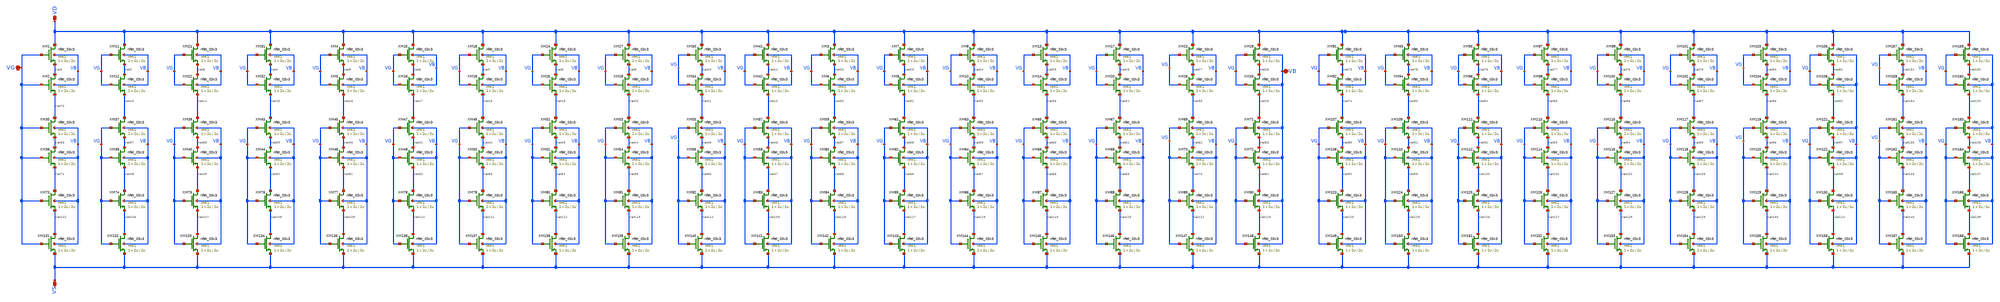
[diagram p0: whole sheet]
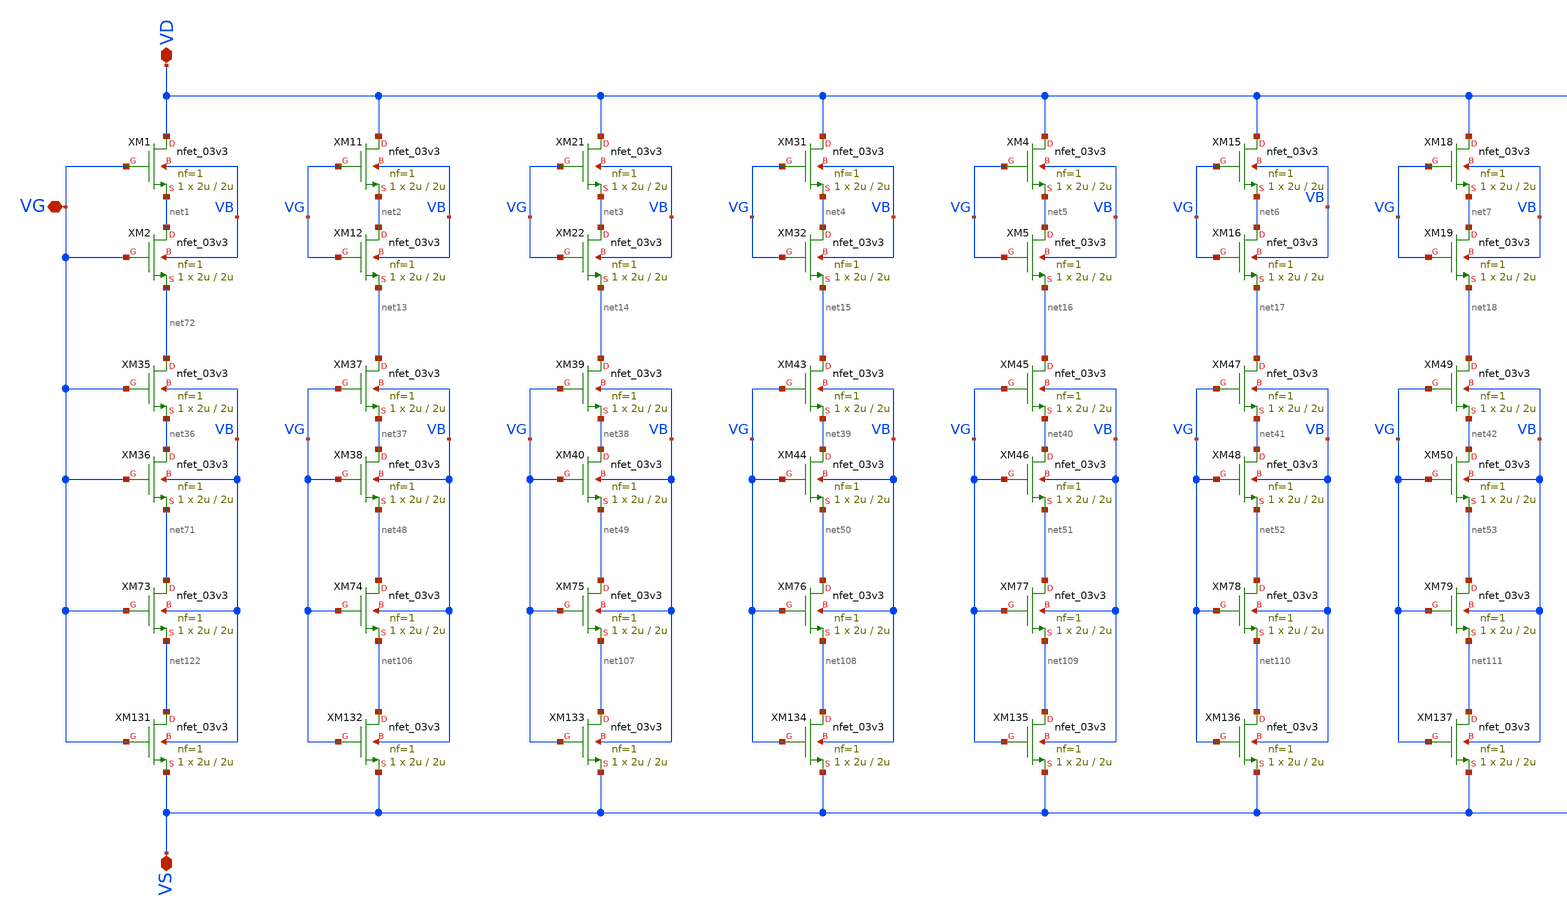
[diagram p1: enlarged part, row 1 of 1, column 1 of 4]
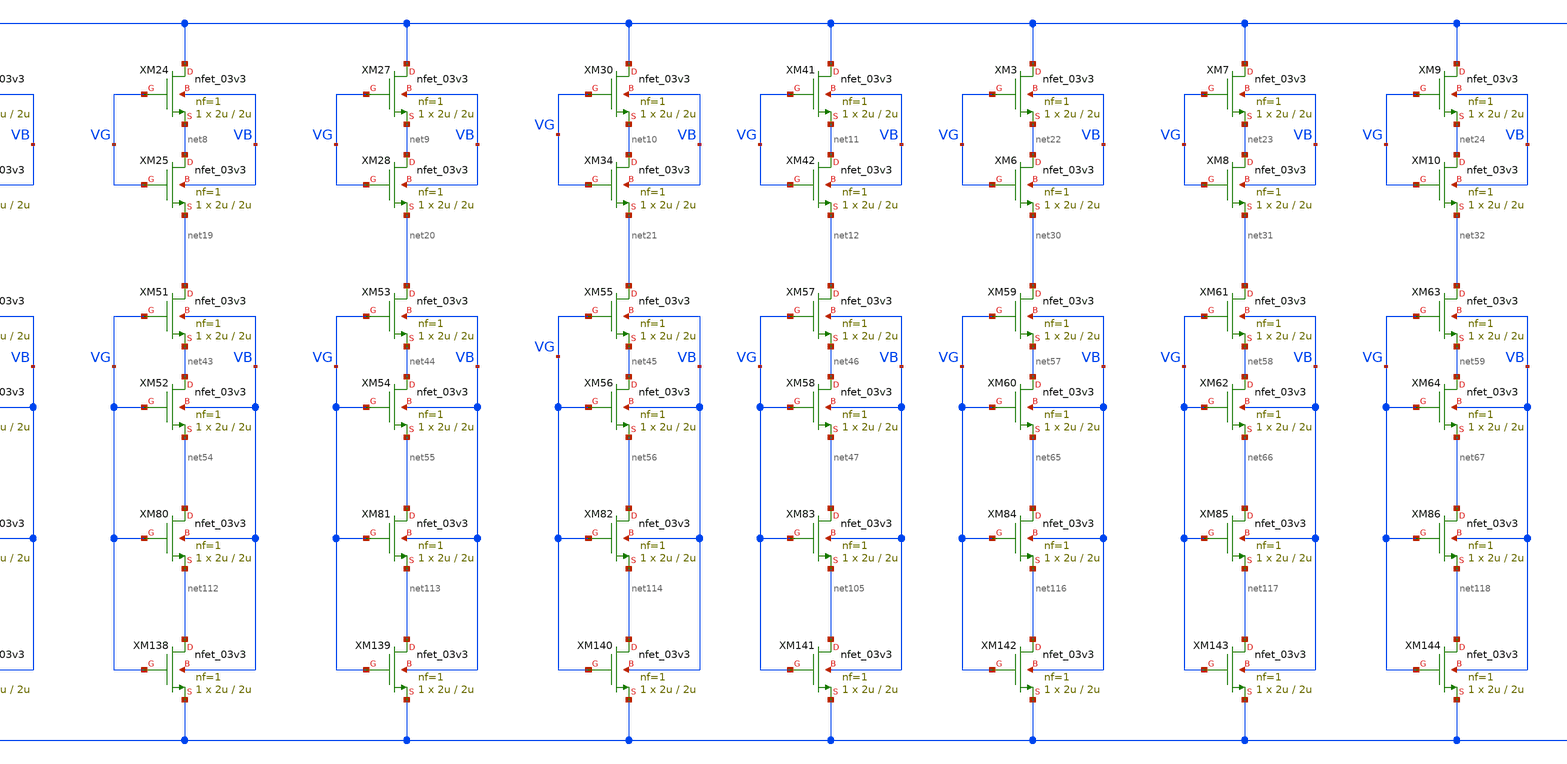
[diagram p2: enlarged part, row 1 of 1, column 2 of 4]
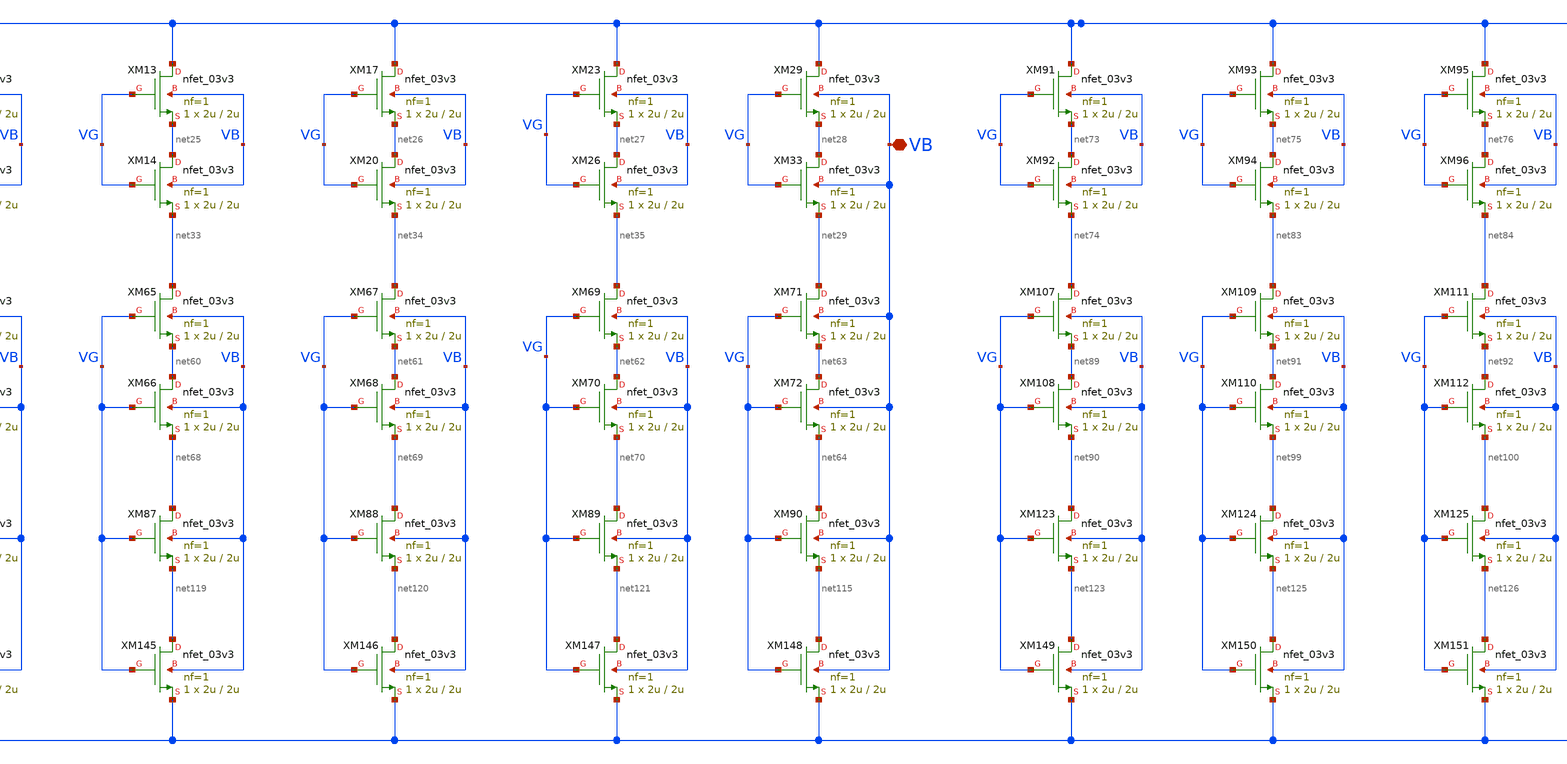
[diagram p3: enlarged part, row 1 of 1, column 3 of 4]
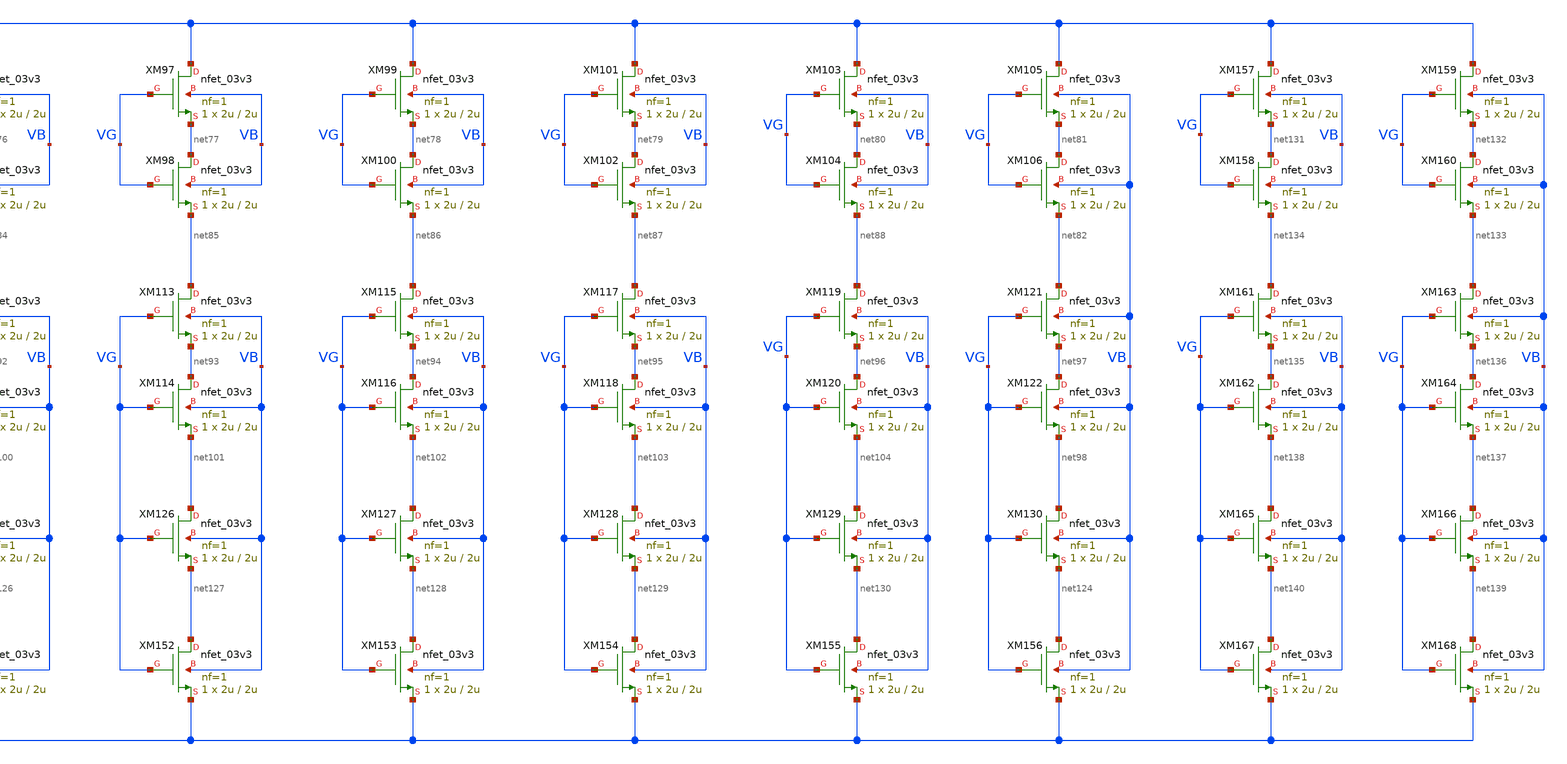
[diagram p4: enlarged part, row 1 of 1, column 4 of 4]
** sch_path: Voltage_Reference/symbols/NMOS_association_18u_5u.sch
**.subckt NMOS_association_18u_5u VD VG VS VB
*.iopin VD
*.iopin VG
*.iopin VS
*.iopin VB
XM1 VD VG net1 VB nfet_03v3 L=2u W=2u nf=1 ad='int((nf+1)/2) * W/nf * 0.18u' as='int((nf+2)/2) * W/nf * 0.18u'
+ pd='2*int((nf+1)/2) * (W/nf + 0.18u)' ps='2*int((nf+2)/2) * (W/nf + 0.18u)' nrd='0.18u / W' nrs='0.18u / W'
+ sa=0 sb=0 sd=0 m=1
XM2 net1 VG net72 VB nfet_03v3 L=2u W=2u nf=1 ad='int((nf+1)/2) * W/nf * 0.18u' as='int((nf+2)/2) * W/nf * 0.18u'
+ pd='2*int((nf+1)/2) * (W/nf + 0.18u)' ps='2*int((nf+2)/2) * (W/nf + 0.18u)' nrd='0.18u / W' nrs='0.18u / W'
+ sa=0 sb=0 sd=0 m=1
XM11 VD VG net2 VB nfet_03v3 L=2u W=2u nf=1 ad='int((nf+1)/2) * W/nf * 0.18u' as='int((nf+2)/2) * W/nf * 0.18u'
+ pd='2*int((nf+1)/2) * (W/nf + 0.18u)' ps='2*int((nf+2)/2) * (W/nf + 0.18u)' nrd='0.18u / W' nrs='0.18u / W'
+ sa=0 sb=0 sd=0 m=1
XM12 net2 VG net13 VB nfet_03v3 L=2u W=2u nf=1 ad='int((nf+1)/2) * W/nf * 0.18u' as='int((nf+2)/2) * W/nf * 0.18u'
+ pd='2*int((nf+1)/2) * (W/nf + 0.18u)' ps='2*int((nf+2)/2) * (W/nf + 0.18u)' nrd='0.18u / W' nrs='0.18u / W'
+ sa=0 sb=0 sd=0 m=1
XM21 VD VG net3 VB nfet_03v3 L=2u W=2u nf=1 ad='int((nf+1)/2) * W/nf * 0.18u' as='int((nf+2)/2) * W/nf * 0.18u'
+ pd='2*int((nf+1)/2) * (W/nf + 0.18u)' ps='2*int((nf+2)/2) * (W/nf + 0.18u)' nrd='0.18u / W' nrs='0.18u / W'
+ sa=0 sb=0 sd=0 m=1
XM22 net3 VG net14 VB nfet_03v3 L=2u W=2u nf=1 ad='int((nf+1)/2) * W/nf * 0.18u' as='int((nf+2)/2) * W/nf * 0.18u'
+ pd='2*int((nf+1)/2) * (W/nf + 0.18u)' ps='2*int((nf+2)/2) * (W/nf + 0.18u)' nrd='0.18u / W' nrs='0.18u / W'
+ sa=0 sb=0 sd=0 m=1
XM31 VD VG net4 VB nfet_03v3 L=2u W=2u nf=1 ad='int((nf+1)/2) * W/nf * 0.18u' as='int((nf+2)/2) * W/nf * 0.18u'
+ pd='2*int((nf+1)/2) * (W/nf + 0.18u)' ps='2*int((nf+2)/2) * (W/nf + 0.18u)' nrd='0.18u / W' nrs='0.18u / W'
+ sa=0 sb=0 sd=0 m=1
XM32 net4 VG net15 VB nfet_03v3 L=2u W=2u nf=1 ad='int((nf+1)/2) * W/nf * 0.18u' as='int((nf+2)/2) * W/nf * 0.18u'
+ pd='2*int((nf+1)/2) * (W/nf + 0.18u)' ps='2*int((nf+2)/2) * (W/nf + 0.18u)' nrd='0.18u / W' nrs='0.18u / W'
+ sa=0 sb=0 sd=0 m=1
XM4 VD VG net5 VB nfet_03v3 L=2u W=2u nf=1 ad='int((nf+1)/2) * W/nf * 0.18u' as='int((nf+2)/2) * W/nf * 0.18u'
+ pd='2*int((nf+1)/2) * (W/nf + 0.18u)' ps='2*int((nf+2)/2) * (W/nf + 0.18u)' nrd='0.18u / W' nrs='0.18u / W'
+ sa=0 sb=0 sd=0 m=1
XM5 net5 VG net16 VB nfet_03v3 L=2u W=2u nf=1 ad='int((nf+1)/2) * W/nf * 0.18u' as='int((nf+2)/2) * W/nf * 0.18u'
+ pd='2*int((nf+1)/2) * (W/nf + 0.18u)' ps='2*int((nf+2)/2) * (W/nf + 0.18u)' nrd='0.18u / W' nrs='0.18u / W'
+ sa=0 sb=0 sd=0 m=1
XM15 VD VG net6 VB nfet_03v3 L=2u W=2u nf=1 ad='int((nf+1)/2) * W/nf * 0.18u' as='int((nf+2)/2) * W/nf * 0.18u'
+ pd='2*int((nf+1)/2) * (W/nf + 0.18u)' ps='2*int((nf+2)/2) * (W/nf + 0.18u)' nrd='0.18u / W' nrs='0.18u / W'
+ sa=0 sb=0 sd=0 m=1
XM16 net6 VG net17 VB nfet_03v3 L=2u W=2u nf=1 ad='int((nf+1)/2) * W/nf * 0.18u' as='int((nf+2)/2) * W/nf * 0.18u'
+ pd='2*int((nf+1)/2) * (W/nf + 0.18u)' ps='2*int((nf+2)/2) * (W/nf + 0.18u)' nrd='0.18u / W' nrs='0.18u / W'
+ sa=0 sb=0 sd=0 m=1
XM18 VD VG net7 VB nfet_03v3 L=2u W=2u nf=1 ad='int((nf+1)/2) * W/nf * 0.18u' as='int((nf+2)/2) * W/nf * 0.18u'
+ pd='2*int((nf+1)/2) * (W/nf + 0.18u)' ps='2*int((nf+2)/2) * (W/nf + 0.18u)' nrd='0.18u / W' nrs='0.18u / W'
+ sa=0 sb=0 sd=0 m=1
XM19 net7 VG net18 VB nfet_03v3 L=2u W=2u nf=1 ad='int((nf+1)/2) * W/nf * 0.18u' as='int((nf+2)/2) * W/nf * 0.18u'
+ pd='2*int((nf+1)/2) * (W/nf + 0.18u)' ps='2*int((nf+2)/2) * (W/nf + 0.18u)' nrd='0.18u / W' nrs='0.18u / W'
+ sa=0 sb=0 sd=0 m=1
XM24 VD VG net8 VB nfet_03v3 L=2u W=2u nf=1 ad='int((nf+1)/2) * W/nf * 0.18u' as='int((nf+2)/2) * W/nf * 0.18u'
+ pd='2*int((nf+1)/2) * (W/nf + 0.18u)' ps='2*int((nf+2)/2) * (W/nf + 0.18u)' nrd='0.18u / W' nrs='0.18u / W'
+ sa=0 sb=0 sd=0 m=1
XM25 net8 VG net19 VB nfet_03v3 L=2u W=2u nf=1 ad='int((nf+1)/2) * W/nf * 0.18u' as='int((nf+2)/2) * W/nf * 0.18u'
+ pd='2*int((nf+1)/2) * (W/nf + 0.18u)' ps='2*int((nf+2)/2) * (W/nf + 0.18u)' nrd='0.18u / W' nrs='0.18u / W'
+ sa=0 sb=0 sd=0 m=1
XM27 VD VG net9 VB nfet_03v3 L=2u W=2u nf=1 ad='int((nf+1)/2) * W/nf * 0.18u' as='int((nf+2)/2) * W/nf * 0.18u'
+ pd='2*int((nf+1)/2) * (W/nf + 0.18u)' ps='2*int((nf+2)/2) * (W/nf + 0.18u)' nrd='0.18u / W' nrs='0.18u / W'
+ sa=0 sb=0 sd=0 m=1
XM28 net9 VG net20 VB nfet_03v3 L=2u W=2u nf=1 ad='int((nf+1)/2) * W/nf * 0.18u' as='int((nf+2)/2) * W/nf * 0.18u'
+ pd='2*int((nf+1)/2) * (W/nf + 0.18u)' ps='2*int((nf+2)/2) * (W/nf + 0.18u)' nrd='0.18u / W' nrs='0.18u / W'
+ sa=0 sb=0 sd=0 m=1
XM30 VD VG net10 VB nfet_03v3 L=2u W=2u nf=1 ad='int((nf+1)/2) * W/nf * 0.18u' as='int((nf+2)/2) * W/nf * 0.18u'
+ pd='2*int((nf+1)/2) * (W/nf + 0.18u)' ps='2*int((nf+2)/2) * (W/nf + 0.18u)' nrd='0.18u / W' nrs='0.18u / W'
+ sa=0 sb=0 sd=0 m=1
XM34 net10 VG net21 VB nfet_03v3 L=2u W=2u nf=1 ad='int((nf+1)/2) * W/nf * 0.18u' as='int((nf+2)/2) * W/nf * 0.18u'
+ pd='2*int((nf+1)/2) * (W/nf + 0.18u)' ps='2*int((nf+2)/2) * (W/nf + 0.18u)' nrd='0.18u / W' nrs='0.18u / W'
+ sa=0 sb=0 sd=0 m=1
XM41 VD VG net11 VB nfet_03v3 L=2u W=2u nf=1 ad='int((nf+1)/2) * W/nf * 0.18u' as='int((nf+2)/2) * W/nf * 0.18u'
+ pd='2*int((nf+1)/2) * (W/nf + 0.18u)' ps='2*int((nf+2)/2) * (W/nf + 0.18u)' nrd='0.18u / W' nrs='0.18u / W'
+ sa=0 sb=0 sd=0 m=1
XM42 net11 VG net12 VB nfet_03v3 L=2u W=2u nf=1 ad='int((nf+1)/2) * W/nf * 0.18u' as='int((nf+2)/2) * W/nf * 0.18u'
+ pd='2*int((nf+1)/2) * (W/nf + 0.18u)' ps='2*int((nf+2)/2) * (W/nf + 0.18u)' nrd='0.18u / W' nrs='0.18u / W'
+ sa=0 sb=0 sd=0 m=1
XM3 VD VG net22 VB nfet_03v3 L=2u W=2u nf=1 ad='int((nf+1)/2) * W/nf * 0.18u' as='int((nf+2)/2) * W/nf * 0.18u'
+ pd='2*int((nf+1)/2) * (W/nf + 0.18u)' ps='2*int((nf+2)/2) * (W/nf + 0.18u)' nrd='0.18u / W' nrs='0.18u / W'
+ sa=0 sb=0 sd=0 m=1
XM6 net22 VG net30 VB nfet_03v3 L=2u W=2u nf=1 ad='int((nf+1)/2) * W/nf * 0.18u' as='int((nf+2)/2) * W/nf * 0.18u'
+ pd='2*int((nf+1)/2) * (W/nf + 0.18u)' ps='2*int((nf+2)/2) * (W/nf + 0.18u)' nrd='0.18u / W' nrs='0.18u / W'
+ sa=0 sb=0 sd=0 m=1
XM7 VD VG net23 VB nfet_03v3 L=2u W=2u nf=1 ad='int((nf+1)/2) * W/nf * 0.18u' as='int((nf+2)/2) * W/nf * 0.18u'
+ pd='2*int((nf+1)/2) * (W/nf + 0.18u)' ps='2*int((nf+2)/2) * (W/nf + 0.18u)' nrd='0.18u / W' nrs='0.18u / W'
+ sa=0 sb=0 sd=0 m=1
XM8 net23 VG net31 VB nfet_03v3 L=2u W=2u nf=1 ad='int((nf+1)/2) * W/nf * 0.18u' as='int((nf+2)/2) * W/nf * 0.18u'
+ pd='2*int((nf+1)/2) * (W/nf + 0.18u)' ps='2*int((nf+2)/2) * (W/nf + 0.18u)' nrd='0.18u / W' nrs='0.18u / W'
+ sa=0 sb=0 sd=0 m=1
XM9 VD VG net24 VB nfet_03v3 L=2u W=2u nf=1 ad='int((nf+1)/2) * W/nf * 0.18u' as='int((nf+2)/2) * W/nf * 0.18u'
+ pd='2*int((nf+1)/2) * (W/nf + 0.18u)' ps='2*int((nf+2)/2) * (W/nf + 0.18u)' nrd='0.18u / W' nrs='0.18u / W'
+ sa=0 sb=0 sd=0 m=1
XM10 net24 VG net32 VB nfet_03v3 L=2u W=2u nf=1 ad='int((nf+1)/2) * W/nf * 0.18u' as='int((nf+2)/2) * W/nf * 0.18u'
+ pd='2*int((nf+1)/2) * (W/nf + 0.18u)' ps='2*int((nf+2)/2) * (W/nf + 0.18u)' nrd='0.18u / W' nrs='0.18u / W'
+ sa=0 sb=0 sd=0 m=1
XM13 VD VG net25 VB nfet_03v3 L=2u W=2u nf=1 ad='int((nf+1)/2) * W/nf * 0.18u' as='int((nf+2)/2) * W/nf * 0.18u'
+ pd='2*int((nf+1)/2) * (W/nf + 0.18u)' ps='2*int((nf+2)/2) * (W/nf + 0.18u)' nrd='0.18u / W' nrs='0.18u / W'
+ sa=0 sb=0 sd=0 m=1
XM14 net25 VG net33 VB nfet_03v3 L=2u W=2u nf=1 ad='int((nf+1)/2) * W/nf * 0.18u' as='int((nf+2)/2) * W/nf * 0.18u'
+ pd='2*int((nf+1)/2) * (W/nf + 0.18u)' ps='2*int((nf+2)/2) * (W/nf + 0.18u)' nrd='0.18u / W' nrs='0.18u / W'
+ sa=0 sb=0 sd=0 m=1
XM17 VD VG net26 VB nfet_03v3 L=2u W=2u nf=1 ad='int((nf+1)/2) * W/nf * 0.18u' as='int((nf+2)/2) * W/nf * 0.18u'
+ pd='2*int((nf+1)/2) * (W/nf + 0.18u)' ps='2*int((nf+2)/2) * (W/nf + 0.18u)' nrd='0.18u / W' nrs='0.18u / W'
+ sa=0 sb=0 sd=0 m=1
XM20 net26 VG net34 VB nfet_03v3 L=2u W=2u nf=1 ad='int((nf+1)/2) * W/nf * 0.18u' as='int((nf+2)/2) * W/nf * 0.18u'
+ pd='2*int((nf+1)/2) * (W/nf + 0.18u)' ps='2*int((nf+2)/2) * (W/nf + 0.18u)' nrd='0.18u / W' nrs='0.18u / W'
+ sa=0 sb=0 sd=0 m=1
XM23 VD VG net27 VB nfet_03v3 L=2u W=2u nf=1 ad='int((nf+1)/2) * W/nf * 0.18u' as='int((nf+2)/2) * W/nf * 0.18u'
+ pd='2*int((nf+1)/2) * (W/nf + 0.18u)' ps='2*int((nf+2)/2) * (W/nf + 0.18u)' nrd='0.18u / W' nrs='0.18u / W'
+ sa=0 sb=0 sd=0 m=1
XM26 net27 VG net35 VB nfet_03v3 L=2u W=2u nf=1 ad='int((nf+1)/2) * W/nf * 0.18u' as='int((nf+2)/2) * W/nf * 0.18u'
+ pd='2*int((nf+1)/2) * (W/nf + 0.18u)' ps='2*int((nf+2)/2) * (W/nf + 0.18u)' nrd='0.18u / W' nrs='0.18u / W'
+ sa=0 sb=0 sd=0 m=1
XM29 VD VG net28 VB nfet_03v3 L=2u W=2u nf=1 ad='int((nf+1)/2) * W/nf * 0.18u' as='int((nf+2)/2) * W/nf * 0.18u'
+ pd='2*int((nf+1)/2) * (W/nf + 0.18u)' ps='2*int((nf+2)/2) * (W/nf + 0.18u)' nrd='0.18u / W' nrs='0.18u / W'
+ sa=0 sb=0 sd=0 m=1
XM33 net28 VG net29 VB nfet_03v3 L=2u W=2u nf=1 ad='int((nf+1)/2) * W/nf * 0.18u' as='int((nf+2)/2) * W/nf * 0.18u'
+ pd='2*int((nf+1)/2) * (W/nf + 0.18u)' ps='2*int((nf+2)/2) * (W/nf + 0.18u)' nrd='0.18u / W' nrs='0.18u / W'
+ sa=0 sb=0 sd=0 m=1
XM35 net72 VG net36 VB nfet_03v3 L=2u W=2u nf=1 ad='int((nf+1)/2) * W/nf * 0.18u' as='int((nf+2)/2) * W/nf * 0.18u'
+ pd='2*int((nf+1)/2) * (W/nf + 0.18u)' ps='2*int((nf+2)/2) * (W/nf + 0.18u)' nrd='0.18u / W' nrs='0.18u / W'
+ sa=0 sb=0 sd=0 m=1
XM36 net36 VG net71 VB nfet_03v3 L=2u W=2u nf=1 ad='int((nf+1)/2) * W/nf * 0.18u' as='int((nf+2)/2) * W/nf * 0.18u'
+ pd='2*int((nf+1)/2) * (W/nf + 0.18u)' ps='2*int((nf+2)/2) * (W/nf + 0.18u)' nrd='0.18u / W' nrs='0.18u / W'
+ sa=0 sb=0 sd=0 m=1
XM37 net13 VG net37 VB nfet_03v3 L=2u W=2u nf=1 ad='int((nf+1)/2) * W/nf * 0.18u' as='int((nf+2)/2) * W/nf * 0.18u'
+ pd='2*int((nf+1)/2) * (W/nf + 0.18u)' ps='2*int((nf+2)/2) * (W/nf + 0.18u)' nrd='0.18u / W' nrs='0.18u / W'
+ sa=0 sb=0 sd=0 m=1
XM38 net37 VG net48 VB nfet_03v3 L=2u W=2u nf=1 ad='int((nf+1)/2) * W/nf * 0.18u' as='int((nf+2)/2) * W/nf * 0.18u'
+ pd='2*int((nf+1)/2) * (W/nf + 0.18u)' ps='2*int((nf+2)/2) * (W/nf + 0.18u)' nrd='0.18u / W' nrs='0.18u / W'
+ sa=0 sb=0 sd=0 m=1
XM39 net14 VG net38 VB nfet_03v3 L=2u W=2u nf=1 ad='int((nf+1)/2) * W/nf * 0.18u' as='int((nf+2)/2) * W/nf * 0.18u'
+ pd='2*int((nf+1)/2) * (W/nf + 0.18u)' ps='2*int((nf+2)/2) * (W/nf + 0.18u)' nrd='0.18u / W' nrs='0.18u / W'
+ sa=0 sb=0 sd=0 m=1
XM40 net38 VG net49 VB nfet_03v3 L=2u W=2u nf=1 ad='int((nf+1)/2) * W/nf * 0.18u' as='int((nf+2)/2) * W/nf * 0.18u'
+ pd='2*int((nf+1)/2) * (W/nf + 0.18u)' ps='2*int((nf+2)/2) * (W/nf + 0.18u)' nrd='0.18u / W' nrs='0.18u / W'
+ sa=0 sb=0 sd=0 m=1
XM43 net15 VG net39 VB nfet_03v3 L=2u W=2u nf=1 ad='int((nf+1)/2) * W/nf * 0.18u' as='int((nf+2)/2) * W/nf * 0.18u'
+ pd='2*int((nf+1)/2) * (W/nf + 0.18u)' ps='2*int((nf+2)/2) * (W/nf + 0.18u)' nrd='0.18u / W' nrs='0.18u / W'
+ sa=0 sb=0 sd=0 m=1
XM44 net39 VG net50 VB nfet_03v3 L=2u W=2u nf=1 ad='int((nf+1)/2) * W/nf * 0.18u' as='int((nf+2)/2) * W/nf * 0.18u'
+ pd='2*int((nf+1)/2) * (W/nf + 0.18u)' ps='2*int((nf+2)/2) * (W/nf + 0.18u)' nrd='0.18u / W' nrs='0.18u / W'
+ sa=0 sb=0 sd=0 m=1
XM45 net16 VG net40 VB nfet_03v3 L=2u W=2u nf=1 ad='int((nf+1)/2) * W/nf * 0.18u' as='int((nf+2)/2) * W/nf * 0.18u'
+ pd='2*int((nf+1)/2) * (W/nf + 0.18u)' ps='2*int((nf+2)/2) * (W/nf + 0.18u)' nrd='0.18u / W' nrs='0.18u / W'
+ sa=0 sb=0 sd=0 m=1
XM46 net40 VG net51 VB nfet_03v3 L=2u W=2u nf=1 ad='int((nf+1)/2) * W/nf * 0.18u' as='int((nf+2)/2) * W/nf * 0.18u'
+ pd='2*int((nf+1)/2) * (W/nf + 0.18u)' ps='2*int((nf+2)/2) * (W/nf + 0.18u)' nrd='0.18u / W' nrs='0.18u / W'
+ sa=0 sb=0 sd=0 m=1
XM47 net17 VG net41 VB nfet_03v3 L=2u W=2u nf=1 ad='int((nf+1)/2) * W/nf * 0.18u' as='int((nf+2)/2) * W/nf * 0.18u'
+ pd='2*int((nf+1)/2) * (W/nf + 0.18u)' ps='2*int((nf+2)/2) * (W/nf + 0.18u)' nrd='0.18u / W' nrs='0.18u / W'
+ sa=0 sb=0 sd=0 m=1
XM48 net41 VG net52 VB nfet_03v3 L=2u W=2u nf=1 ad='int((nf+1)/2) * W/nf * 0.18u' as='int((nf+2)/2) * W/nf * 0.18u'
+ pd='2*int((nf+1)/2) * (W/nf + 0.18u)' ps='2*int((nf+2)/2) * (W/nf + 0.18u)' nrd='0.18u / W' nrs='0.18u / W'
+ sa=0 sb=0 sd=0 m=1
XM49 net18 VG net42 VB nfet_03v3 L=2u W=2u nf=1 ad='int((nf+1)/2) * W/nf * 0.18u' as='int((nf+2)/2) * W/nf * 0.18u'
+ pd='2*int((nf+1)/2) * (W/nf + 0.18u)' ps='2*int((nf+2)/2) * (W/nf + 0.18u)' nrd='0.18u / W' nrs='0.18u / W'
+ sa=0 sb=0 sd=0 m=1
XM50 net42 VG net53 VB nfet_03v3 L=2u W=2u nf=1 ad='int((nf+1)/2) * W/nf * 0.18u' as='int((nf+2)/2) * W/nf * 0.18u'
+ pd='2*int((nf+1)/2) * (W/nf + 0.18u)' ps='2*int((nf+2)/2) * (W/nf + 0.18u)' nrd='0.18u / W' nrs='0.18u / W'
+ sa=0 sb=0 sd=0 m=1
XM51 net19 VG net43 VB nfet_03v3 L=2u W=2u nf=1 ad='int((nf+1)/2) * W/nf * 0.18u' as='int((nf+2)/2) * W/nf * 0.18u'
+ pd='2*int((nf+1)/2) * (W/nf + 0.18u)' ps='2*int((nf+2)/2) * (W/nf + 0.18u)' nrd='0.18u / W' nrs='0.18u / W'
+ sa=0 sb=0 sd=0 m=1
XM52 net43 VG net54 VB nfet_03v3 L=2u W=2u nf=1 ad='int((nf+1)/2) * W/nf * 0.18u' as='int((nf+2)/2) * W/nf * 0.18u'
+ pd='2*int((nf+1)/2) * (W/nf + 0.18u)' ps='2*int((nf+2)/2) * (W/nf + 0.18u)' nrd='0.18u / W' nrs='0.18u / W'
+ sa=0 sb=0 sd=0 m=1
XM53 net20 VG net44 VB nfet_03v3 L=2u W=2u nf=1 ad='int((nf+1)/2) * W/nf * 0.18u' as='int((nf+2)/2) * W/nf * 0.18u'
+ pd='2*int((nf+1)/2) * (W/nf + 0.18u)' ps='2*int((nf+2)/2) * (W/nf + 0.18u)' nrd='0.18u / W' nrs='0.18u / W'
+ sa=0 sb=0 sd=0 m=1
XM54 net44 VG net55 VB nfet_03v3 L=2u W=2u nf=1 ad='int((nf+1)/2) * W/nf * 0.18u' as='int((nf+2)/2) * W/nf * 0.18u'
+ pd='2*int((nf+1)/2) * (W/nf + 0.18u)' ps='2*int((nf+2)/2) * (W/nf + 0.18u)' nrd='0.18u / W' nrs='0.18u / W'
+ sa=0 sb=0 sd=0 m=1
XM55 net21 VG net45 VB nfet_03v3 L=2u W=2u nf=1 ad='int((nf+1)/2) * W/nf * 0.18u' as='int((nf+2)/2) * W/nf * 0.18u'
+ pd='2*int((nf+1)/2) * (W/nf + 0.18u)' ps='2*int((nf+2)/2) * (W/nf + 0.18u)' nrd='0.18u / W' nrs='0.18u / W'
+ sa=0 sb=0 sd=0 m=1
XM56 net45 VG net56 VB nfet_03v3 L=2u W=2u nf=1 ad='int((nf+1)/2) * W/nf * 0.18u' as='int((nf+2)/2) * W/nf * 0.18u'
+ pd='2*int((nf+1)/2) * (W/nf + 0.18u)' ps='2*int((nf+2)/2) * (W/nf + 0.18u)' nrd='0.18u / W' nrs='0.18u / W'
+ sa=0 sb=0 sd=0 m=1
XM57 net12 VG net46 VB nfet_03v3 L=2u W=2u nf=1 ad='int((nf+1)/2) * W/nf * 0.18u' as='int((nf+2)/2) * W/nf * 0.18u'
+ pd='2*int((nf+1)/2) * (W/nf + 0.18u)' ps='2*int((nf+2)/2) * (W/nf + 0.18u)' nrd='0.18u / W' nrs='0.18u / W'
+ sa=0 sb=0 sd=0 m=1
XM58 net46 VG net47 VB nfet_03v3 L=2u W=2u nf=1 ad='int((nf+1)/2) * W/nf * 0.18u' as='int((nf+2)/2) * W/nf * 0.18u'
+ pd='2*int((nf+1)/2) * (W/nf + 0.18u)' ps='2*int((nf+2)/2) * (W/nf + 0.18u)' nrd='0.18u / W' nrs='0.18u / W'
+ sa=0 sb=0 sd=0 m=1
XM59 net30 VG net57 VB nfet_03v3 L=2u W=2u nf=1 ad='int((nf+1)/2) * W/nf * 0.18u' as='int((nf+2)/2) * W/nf * 0.18u'
+ pd='2*int((nf+1)/2) * (W/nf + 0.18u)' ps='2*int((nf+2)/2) * (W/nf + 0.18u)' nrd='0.18u / W' nrs='0.18u / W'
+ sa=0 sb=0 sd=0 m=1
XM60 net57 VG net65 VB nfet_03v3 L=2u W=2u nf=1 ad='int((nf+1)/2) * W/nf * 0.18u' as='int((nf+2)/2) * W/nf * 0.18u'
+ pd='2*int((nf+1)/2) * (W/nf + 0.18u)' ps='2*int((nf+2)/2) * (W/nf + 0.18u)' nrd='0.18u / W' nrs='0.18u / W'
+ sa=0 sb=0 sd=0 m=1
XM61 net31 VG net58 VB nfet_03v3 L=2u W=2u nf=1 ad='int((nf+1)/2) * W/nf * 0.18u' as='int((nf+2)/2) * W/nf * 0.18u'
+ pd='2*int((nf+1)/2) * (W/nf + 0.18u)' ps='2*int((nf+2)/2) * (W/nf + 0.18u)' nrd='0.18u / W' nrs='0.18u / W'
+ sa=0 sb=0 sd=0 m=1
XM62 net58 VG net66 VB nfet_03v3 L=2u W=2u nf=1 ad='int((nf+1)/2) * W/nf * 0.18u' as='int((nf+2)/2) * W/nf * 0.18u'
+ pd='2*int((nf+1)/2) * (W/nf + 0.18u)' ps='2*int((nf+2)/2) * (W/nf + 0.18u)' nrd='0.18u / W' nrs='0.18u / W'
+ sa=0 sb=0 sd=0 m=1
XM63 net32 VG net59 VB nfet_03v3 L=2u W=2u nf=1 ad='int((nf+1)/2) * W/nf * 0.18u' as='int((nf+2)/2) * W/nf * 0.18u'
+ pd='2*int((nf+1)/2) * (W/nf + 0.18u)' ps='2*int((nf+2)/2) * (W/nf + 0.18u)' nrd='0.18u / W' nrs='0.18u / W'
+ sa=0 sb=0 sd=0 m=1
XM64 net59 VG net67 VB nfet_03v3 L=2u W=2u nf=1 ad='int((nf+1)/2) * W/nf * 0.18u' as='int((nf+2)/2) * W/nf * 0.18u'
+ pd='2*int((nf+1)/2) * (W/nf + 0.18u)' ps='2*int((nf+2)/2) * (W/nf + 0.18u)' nrd='0.18u / W' nrs='0.18u / W'
+ sa=0 sb=0 sd=0 m=1
XM65 net33 VG net60 VB nfet_03v3 L=2u W=2u nf=1 ad='int((nf+1)/2) * W/nf * 0.18u' as='int((nf+2)/2) * W/nf * 0.18u'
+ pd='2*int((nf+1)/2) * (W/nf + 0.18u)' ps='2*int((nf+2)/2) * (W/nf + 0.18u)' nrd='0.18u / W' nrs='0.18u / W'
+ sa=0 sb=0 sd=0 m=1
XM66 net60 VG net68 VB nfet_03v3 L=2u W=2u nf=1 ad='int((nf+1)/2) * W/nf * 0.18u' as='int((nf+2)/2) * W/nf * 0.18u'
+ pd='2*int((nf+1)/2) * (W/nf + 0.18u)' ps='2*int((nf+2)/2) * (W/nf + 0.18u)' nrd='0.18u / W' nrs='0.18u / W'
+ sa=0 sb=0 sd=0 m=1
XM67 net34 VG net61 VB nfet_03v3 L=2u W=2u nf=1 ad='int((nf+1)/2) * W/nf * 0.18u' as='int((nf+2)/2) * W/nf * 0.18u'
+ pd='2*int((nf+1)/2) * (W/nf + 0.18u)' ps='2*int((nf+2)/2) * (W/nf + 0.18u)' nrd='0.18u / W' nrs='0.18u / W'
+ sa=0 sb=0 sd=0 m=1
XM68 net61 VG net69 VB nfet_03v3 L=2u W=2u nf=1 ad='int((nf+1)/2) * W/nf * 0.18u' as='int((nf+2)/2) * W/nf * 0.18u'
+ pd='2*int((nf+1)/2) * (W/nf + 0.18u)' ps='2*int((nf+2)/2) * (W/nf + 0.18u)' nrd='0.18u / W' nrs='0.18u / W'
+ sa=0 sb=0 sd=0 m=1
XM69 net35 VG net62 VB nfet_03v3 L=2u W=2u nf=1 ad='int((nf+1)/2) * W/nf * 0.18u' as='int((nf+2)/2) * W/nf * 0.18u'
+ pd='2*int((nf+1)/2) * (W/nf + 0.18u)' ps='2*int((nf+2)/2) * (W/nf + 0.18u)' nrd='0.18u / W' nrs='0.18u / W'
+ sa=0 sb=0 sd=0 m=1
XM70 net62 VG net70 VB nfet_03v3 L=2u W=2u nf=1 ad='int((nf+1)/2) * W/nf * 0.18u' as='int((nf+2)/2) * W/nf * 0.18u'
+ pd='2*int((nf+1)/2) * (W/nf + 0.18u)' ps='2*int((nf+2)/2) * (W/nf + 0.18u)' nrd='0.18u / W' nrs='0.18u / W'
+ sa=0 sb=0 sd=0 m=1
XM71 net29 VG net63 VB nfet_03v3 L=2u W=2u nf=1 ad='int((nf+1)/2) * W/nf * 0.18u' as='int((nf+2)/2) * W/nf * 0.18u'
+ pd='2*int((nf+1)/2) * (W/nf + 0.18u)' ps='2*int((nf+2)/2) * (W/nf + 0.18u)' nrd='0.18u / W' nrs='0.18u / W'
+ sa=0 sb=0 sd=0 m=1
XM72 net63 VG net64 VB nfet_03v3 L=2u W=2u nf=1 ad='int((nf+1)/2) * W/nf * 0.18u' as='int((nf+2)/2) * W/nf * 0.18u'
+ pd='2*int((nf+1)/2) * (W/nf + 0.18u)' ps='2*int((nf+2)/2) * (W/nf + 0.18u)' nrd='0.18u / W' nrs='0.18u / W'
+ sa=0 sb=0 sd=0 m=1
XM73 net71 VG net122 VB nfet_03v3 L=2u W=2u nf=1 ad='int((nf+1)/2) * W/nf * 0.18u' as='int((nf+2)/2) * W/nf * 0.18u'
+ pd='2*int((nf+1)/2) * (W/nf + 0.18u)' ps='2*int((nf+2)/2) * (W/nf + 0.18u)' nrd='0.18u / W' nrs='0.18u / W'
+ sa=0 sb=0 sd=0 m=1
XM74 net48 VG net106 VB nfet_03v3 L=2u W=2u nf=1 ad='int((nf+1)/2) * W/nf * 0.18u' as='int((nf+2)/2) * W/nf * 0.18u'
+ pd='2*int((nf+1)/2) * (W/nf + 0.18u)' ps='2*int((nf+2)/2) * (W/nf + 0.18u)' nrd='0.18u / W' nrs='0.18u / W'
+ sa=0 sb=0 sd=0 m=1
XM75 net49 VG net107 VB nfet_03v3 L=2u W=2u nf=1 ad='int((nf+1)/2) * W/nf * 0.18u' as='int((nf+2)/2) * W/nf * 0.18u'
+ pd='2*int((nf+1)/2) * (W/nf + 0.18u)' ps='2*int((nf+2)/2) * (W/nf + 0.18u)' nrd='0.18u / W' nrs='0.18u / W'
+ sa=0 sb=0 sd=0 m=1
XM76 net50 VG net108 VB nfet_03v3 L=2u W=2u nf=1 ad='int((nf+1)/2) * W/nf * 0.18u' as='int((nf+2)/2) * W/nf * 0.18u'
+ pd='2*int((nf+1)/2) * (W/nf + 0.18u)' ps='2*int((nf+2)/2) * (W/nf + 0.18u)' nrd='0.18u / W' nrs='0.18u / W'
+ sa=0 sb=0 sd=0 m=1
XM77 net51 VG net109 VB nfet_03v3 L=2u W=2u nf=1 ad='int((nf+1)/2) * W/nf * 0.18u' as='int((nf+2)/2) * W/nf * 0.18u'
+ pd='2*int((nf+1)/2) * (W/nf + 0.18u)' ps='2*int((nf+2)/2) * (W/nf + 0.18u)' nrd='0.18u / W' nrs='0.18u / W'
+ sa=0 sb=0 sd=0 m=1
XM78 net52 VG net110 VB nfet_03v3 L=2u W=2u nf=1 ad='int((nf+1)/2) * W/nf * 0.18u' as='int((nf+2)/2) * W/nf * 0.18u'
+ pd='2*int((nf+1)/2) * (W/nf + 0.18u)' ps='2*int((nf+2)/2) * (W/nf + 0.18u)' nrd='0.18u / W' nrs='0.18u / W'
+ sa=0 sb=0 sd=0 m=1
XM79 net53 VG net111 VB nfet_03v3 L=2u W=2u nf=1 ad='int((nf+1)/2) * W/nf * 0.18u' as='int((nf+2)/2) * W/nf * 0.18u'
+ pd='2*int((nf+1)/2) * (W/nf + 0.18u)' ps='2*int((nf+2)/2) * (W/nf + 0.18u)' nrd='0.18u / W' nrs='0.18u / W'
+ sa=0 sb=0 sd=0 m=1
XM80 net54 VG net112 VB nfet_03v3 L=2u W=2u nf=1 ad='int((nf+1)/2) * W/nf * 0.18u' as='int((nf+2)/2) * W/nf * 0.18u'
+ pd='2*int((nf+1)/2) * (W/nf + 0.18u)' ps='2*int((nf+2)/2) * (W/nf + 0.18u)' nrd='0.18u / W' nrs='0.18u / W'
+ sa=0 sb=0 sd=0 m=1
XM81 net55 VG net113 VB nfet_03v3 L=2u W=2u nf=1 ad='int((nf+1)/2) * W/nf * 0.18u' as='int((nf+2)/2) * W/nf * 0.18u'
+ pd='2*int((nf+1)/2) * (W/nf + 0.18u)' ps='2*int((nf+2)/2) * (W/nf + 0.18u)' nrd='0.18u / W' nrs='0.18u / W'
+ sa=0 sb=0 sd=0 m=1
XM82 net56 VG net114 VB nfet_03v3 L=2u W=2u nf=1 ad='int((nf+1)/2) * W/nf * 0.18u' as='int((nf+2)/2) * W/nf * 0.18u'
+ pd='2*int((nf+1)/2) * (W/nf + 0.18u)' ps='2*int((nf+2)/2) * (W/nf + 0.18u)' nrd='0.18u / W' nrs='0.18u / W'
+ sa=0 sb=0 sd=0 m=1
XM83 net47 VG net105 VB nfet_03v3 L=2u W=2u nf=1 ad='int((nf+1)/2) * W/nf * 0.18u' as='int((nf+2)/2) * W/nf * 0.18u'
+ pd='2*int((nf+1)/2) * (W/nf + 0.18u)' ps='2*int((nf+2)/2) * (W/nf + 0.18u)' nrd='0.18u / W' nrs='0.18u / W'
+ sa=0 sb=0 sd=0 m=1
XM84 net65 VG net116 VB nfet_03v3 L=2u W=2u nf=1 ad='int((nf+1)/2) * W/nf * 0.18u' as='int((nf+2)/2) * W/nf * 0.18u'
+ pd='2*int((nf+1)/2) * (W/nf + 0.18u)' ps='2*int((nf+2)/2) * (W/nf + 0.18u)' nrd='0.18u / W' nrs='0.18u / W'
+ sa=0 sb=0 sd=0 m=1
XM85 net66 VG net117 VB nfet_03v3 L=2u W=2u nf=1 ad='int((nf+1)/2) * W/nf * 0.18u' as='int((nf+2)/2) * W/nf * 0.18u'
+ pd='2*int((nf+1)/2) * (W/nf + 0.18u)' ps='2*int((nf+2)/2) * (W/nf + 0.18u)' nrd='0.18u / W' nrs='0.18u / W'
+ sa=0 sb=0 sd=0 m=1
XM86 net67 VG net118 VB nfet_03v3 L=2u W=2u nf=1 ad='int((nf+1)/2) * W/nf * 0.18u' as='int((nf+2)/2) * W/nf * 0.18u'
+ pd='2*int((nf+1)/2) * (W/nf + 0.18u)' ps='2*int((nf+2)/2) * (W/nf + 0.18u)' nrd='0.18u / W' nrs='0.18u / W'
+ sa=0 sb=0 sd=0 m=1
XM87 net68 VG net119 VB nfet_03v3 L=2u W=2u nf=1 ad='int((nf+1)/2) * W/nf * 0.18u' as='int((nf+2)/2) * W/nf * 0.18u'
+ pd='2*int((nf+1)/2) * (W/nf + 0.18u)' ps='2*int((nf+2)/2) * (W/nf + 0.18u)' nrd='0.18u / W' nrs='0.18u / W'
+ sa=0 sb=0 sd=0 m=1
XM88 net69 VG net120 VB nfet_03v3 L=2u W=2u nf=1 ad='int((nf+1)/2) * W/nf * 0.18u' as='int((nf+2)/2) * W/nf * 0.18u'
+ pd='2*int((nf+1)/2) * (W/nf + 0.18u)' ps='2*int((nf+2)/2) * (W/nf + 0.18u)' nrd='0.18u / W' nrs='0.18u / W'
+ sa=0 sb=0 sd=0 m=1
XM89 net70 VG net121 VB nfet_03v3 L=2u W=2u nf=1 ad='int((nf+1)/2) * W/nf * 0.18u' as='int((nf+2)/2) * W/nf * 0.18u'
+ pd='2*int((nf+1)/2) * (W/nf + 0.18u)' ps='2*int((nf+2)/2) * (W/nf + 0.18u)' nrd='0.18u / W' nrs='0.18u / W'
+ sa=0 sb=0 sd=0 m=1
XM90 net64 VG net115 VB nfet_03v3 L=2u W=2u nf=1 ad='int((nf+1)/2) * W/nf * 0.18u' as='int((nf+2)/2) * W/nf * 0.18u'
+ pd='2*int((nf+1)/2) * (W/nf + 0.18u)' ps='2*int((nf+2)/2) * (W/nf + 0.18u)' nrd='0.18u / W' nrs='0.18u / W'
+ sa=0 sb=0 sd=0 m=1
XM91 VD VG net73 VB nfet_03v3 L=2u W=2u nf=1 ad='int((nf+1)/2) * W/nf * 0.18u' as='int((nf+2)/2) * W/nf * 0.18u'
+ pd='2*int((nf+1)/2) * (W/nf + 0.18u)' ps='2*int((nf+2)/2) * (W/nf + 0.18u)' nrd='0.18u / W' nrs='0.18u / W'
+ sa=0 sb=0 sd=0 m=1
XM92 net73 VG net74 VB nfet_03v3 L=2u W=2u nf=1 ad='int((nf+1)/2) * W/nf * 0.18u' as='int((nf+2)/2) * W/nf * 0.18u'
+ pd='2*int((nf+1)/2) * (W/nf + 0.18u)' ps='2*int((nf+2)/2) * (W/nf + 0.18u)' nrd='0.18u / W' nrs='0.18u / W'
+ sa=0 sb=0 sd=0 m=1
XM93 VD VG net75 VB nfet_03v3 L=2u W=2u nf=1 ad='int((nf+1)/2) * W/nf * 0.18u' as='int((nf+2)/2) * W/nf * 0.18u'
+ pd='2*int((nf+1)/2) * (W/nf + 0.18u)' ps='2*int((nf+2)/2) * (W/nf + 0.18u)' nrd='0.18u / W' nrs='0.18u / W'
+ sa=0 sb=0 sd=0 m=1
XM94 net75 VG net83 VB nfet_03v3 L=2u W=2u nf=1 ad='int((nf+1)/2) * W/nf * 0.18u' as='int((nf+2)/2) * W/nf * 0.18u'
+ pd='2*int((nf+1)/2) * (W/nf + 0.18u)' ps='2*int((nf+2)/2) * (W/nf + 0.18u)' nrd='0.18u / W' nrs='0.18u / W'
+ sa=0 sb=0 sd=0 m=1
XM95 VD VG net76 VB nfet_03v3 L=2u W=2u nf=1 ad='int((nf+1)/2) * W/nf * 0.18u' as='int((nf+2)/2) * W/nf * 0.18u'
+ pd='2*int((nf+1)/2) * (W/nf + 0.18u)' ps='2*int((nf+2)/2) * (W/nf + 0.18u)' nrd='0.18u / W' nrs='0.18u / W'
+ sa=0 sb=0 sd=0 m=1
XM96 net76 VG net84 VB nfet_03v3 L=2u W=2u nf=1 ad='int((nf+1)/2) * W/nf * 0.18u' as='int((nf+2)/2) * W/nf * 0.18u'
+ pd='2*int((nf+1)/2) * (W/nf + 0.18u)' ps='2*int((nf+2)/2) * (W/nf + 0.18u)' nrd='0.18u / W' nrs='0.18u / W'
+ sa=0 sb=0 sd=0 m=1
XM97 VD VG net77 VB nfet_03v3 L=2u W=2u nf=1 ad='int((nf+1)/2) * W/nf * 0.18u' as='int((nf+2)/2) * W/nf * 0.18u'
+ pd='2*int((nf+1)/2) * (W/nf + 0.18u)' ps='2*int((nf+2)/2) * (W/nf + 0.18u)' nrd='0.18u / W' nrs='0.18u / W'
+ sa=0 sb=0 sd=0 m=1
XM98 net77 VG net85 VB nfet_03v3 L=2u W=2u nf=1 ad='int((nf+1)/2) * W/nf * 0.18u' as='int((nf+2)/2) * W/nf * 0.18u'
+ pd='2*int((nf+1)/2) * (W/nf + 0.18u)' ps='2*int((nf+2)/2) * (W/nf + 0.18u)' nrd='0.18u / W' nrs='0.18u / W'
+ sa=0 sb=0 sd=0 m=1
XM99 VD VG net78 VB nfet_03v3 L=2u W=2u nf=1 ad='int((nf+1)/2) * W/nf * 0.18u' as='int((nf+2)/2) * W/nf * 0.18u'
+ pd='2*int((nf+1)/2) * (W/nf + 0.18u)' ps='2*int((nf+2)/2) * (W/nf + 0.18u)' nrd='0.18u / W' nrs='0.18u / W'
+ sa=0 sb=0 sd=0 m=1
XM100 net78 VG net86 VB nfet_03v3 L=2u W=2u nf=1 ad='int((nf+1)/2) * W/nf * 0.18u' as='int((nf+2)/2) * W/nf * 0.18u'
+ pd='2*int((nf+1)/2) * (W/nf + 0.18u)' ps='2*int((nf+2)/2) * (W/nf + 0.18u)' nrd='0.18u / W' nrs='0.18u / W'
+ sa=0 sb=0 sd=0 m=1
XM101 VD VG net79 VB nfet_03v3 L=2u W=2u nf=1 ad='int((nf+1)/2) * W/nf * 0.18u' as='int((nf+2)/2) * W/nf * 0.18u'
+ pd='2*int((nf+1)/2) * (W/nf + 0.18u)' ps='2*int((nf+2)/2) * (W/nf + 0.18u)' nrd='0.18u / W' nrs='0.18u / W'
+ sa=0 sb=0 sd=0 m=1
XM102 net79 VG net87 VB nfet_03v3 L=2u W=2u nf=1 ad='int((nf+1)/2) * W/nf * 0.18u' as='int((nf+2)/2) * W/nf * 0.18u'
+ pd='2*int((nf+1)/2) * (W/nf + 0.18u)' ps='2*int((nf+2)/2) * (W/nf + 0.18u)' nrd='0.18u / W' nrs='0.18u / W'
+ sa=0 sb=0 sd=0 m=1
XM103 VD VG net80 VB nfet_03v3 L=2u W=2u nf=1 ad='int((nf+1)/2) * W/nf * 0.18u' as='int((nf+2)/2) * W/nf * 0.18u'
+ pd='2*int((nf+1)/2) * (W/nf + 0.18u)' ps='2*int((nf+2)/2) * (W/nf + 0.18u)' nrd='0.18u / W' nrs='0.18u / W'
+ sa=0 sb=0 sd=0 m=1
XM104 net80 VG net88 VB nfet_03v3 L=2u W=2u nf=1 ad='int((nf+1)/2) * W/nf * 0.18u' as='int((nf+2)/2) * W/nf * 0.18u'
+ pd='2*int((nf+1)/2) * (W/nf + 0.18u)' ps='2*int((nf+2)/2) * (W/nf + 0.18u)' nrd='0.18u / W' nrs='0.18u / W'
+ sa=0 sb=0 sd=0 m=1
XM105 VD VG net81 VB nfet_03v3 L=2u W=2u nf=1 ad='int((nf+1)/2) * W/nf * 0.18u' as='int((nf+2)/2) * W/nf * 0.18u'
+ pd='2*int((nf+1)/2) * (W/nf + 0.18u)' ps='2*int((nf+2)/2) * (W/nf + 0.18u)' nrd='0.18u / W' nrs='0.18u / W'
+ sa=0 sb=0 sd=0 m=1
XM106 net81 VG net82 VB nfet_03v3 L=2u W=2u nf=1 ad='int((nf+1)/2) * W/nf * 0.18u' as='int((nf+2)/2) * W/nf * 0.18u'
+ pd='2*int((nf+1)/2) * (W/nf + 0.18u)' ps='2*int((nf+2)/2) * (W/nf + 0.18u)' nrd='0.18u / W' nrs='0.18u / W'
+ sa=0 sb=0 sd=0 m=1
XM107 net74 VG net89 VB nfet_03v3 L=2u W=2u nf=1 ad='int((nf+1)/2) * W/nf * 0.18u' as='int((nf+2)/2) * W/nf * 0.18u'
+ pd='2*int((nf+1)/2) * (W/nf + 0.18u)' ps='2*int((nf+2)/2) * (W/nf + 0.18u)' nrd='0.18u / W' nrs='0.18u / W'
+ sa=0 sb=0 sd=0 m=1
XM108 net89 VG net90 VB nfet_03v3 L=2u W=2u nf=1 ad='int((nf+1)/2) * W/nf * 0.18u' as='int((nf+2)/2) * W/nf * 0.18u'
+ pd='2*int((nf+1)/2) * (W/nf + 0.18u)' ps='2*int((nf+2)/2) * (W/nf + 0.18u)' nrd='0.18u / W' nrs='0.18u / W'
+ sa=0 sb=0 sd=0 m=1
XM109 net83 VG net91 VB nfet_03v3 L=2u W=2u nf=1 ad='int((nf+1)/2) * W/nf * 0.18u' as='int((nf+2)/2) * W/nf * 0.18u'
+ pd='2*int((nf+1)/2) * (W/nf + 0.18u)' ps='2*int((nf+2)/2) * (W/nf + 0.18u)' nrd='0.18u / W' nrs='0.18u / W'
+ sa=0 sb=0 sd=0 m=1
XM110 net91 VG net99 VB nfet_03v3 L=2u W=2u nf=1 ad='int((nf+1)/2) * W/nf * 0.18u' as='int((nf+2)/2) * W/nf * 0.18u'
+ pd='2*int((nf+1)/2) * (W/nf + 0.18u)' ps='2*int((nf+2)/2) * (W/nf + 0.18u)' nrd='0.18u / W' nrs='0.18u / W'
+ sa=0 sb=0 sd=0 m=1
XM111 net84 VG net92 VB nfet_03v3 L=2u W=2u nf=1 ad='int((nf+1)/2) * W/nf * 0.18u' as='int((nf+2)/2) * W/nf * 0.18u'
+ pd='2*int((nf+1)/2) * (W/nf + 0.18u)' ps='2*int((nf+2)/2) * (W/nf + 0.18u)' nrd='0.18u / W' nrs='0.18u / W'
+ sa=0 sb=0 sd=0 m=1
XM112 net92 VG net100 VB nfet_03v3 L=2u W=2u nf=1 ad='int((nf+1)/2) * W/nf * 0.18u' as='int((nf+2)/2) * W/nf * 0.18u'
+ pd='2*int((nf+1)/2) * (W/nf + 0.18u)' ps='2*int((nf+2)/2) * (W/nf + 0.18u)' nrd='0.18u / W' nrs='0.18u / W'
+ sa=0 sb=0 sd=0 m=1
XM113 net85 VG net93 VB nfet_03v3 L=2u W=2u nf=1 ad='int((nf+1)/2) * W/nf * 0.18u' as='int((nf+2)/2) * W/nf * 0.18u'
+ pd='2*int((nf+1)/2) * (W/nf + 0.18u)' ps='2*int((nf+2)/2) * (W/nf + 0.18u)' nrd='0.18u / W' nrs='0.18u / W'
+ sa=0 sb=0 sd=0 m=1
XM114 net93 VG net101 VB nfet_03v3 L=2u W=2u nf=1 ad='int((nf+1)/2) * W/nf * 0.18u' as='int((nf+2)/2) * W/nf * 0.18u'
+ pd='2*int((nf+1)/2) * (W/nf + 0.18u)' ps='2*int((nf+2)/2) * (W/nf + 0.18u)' nrd='0.18u / W' nrs='0.18u / W'
+ sa=0 sb=0 sd=0 m=1
XM115 net86 VG net94 VB nfet_03v3 L=2u W=2u nf=1 ad='int((nf+1)/2) * W/nf * 0.18u' as='int((nf+2)/2) * W/nf * 0.18u'
+ pd='2*int((nf+1)/2) * (W/nf + 0.18u)' ps='2*int((nf+2)/2) * (W/nf + 0.18u)' nrd='0.18u / W' nrs='0.18u / W'
+ sa=0 sb=0 sd=0 m=1
XM116 net94 VG net102 VB nfet_03v3 L=2u W=2u nf=1 ad='int((nf+1)/2) * W/nf * 0.18u' as='int((nf+2)/2) * W/nf * 0.18u'
+ pd='2*int((nf+1)/2) * (W/nf + 0.18u)' ps='2*int((nf+2)/2) * (W/nf + 0.18u)' nrd='0.18u / W' nrs='0.18u / W'
+ sa=0 sb=0 sd=0 m=1
XM117 net87 VG net95 VB nfet_03v3 L=2u W=2u nf=1 ad='int((nf+1)/2) * W/nf * 0.18u' as='int((nf+2)/2) * W/nf * 0.18u'
+ pd='2*int((nf+1)/2) * (W/nf + 0.18u)' ps='2*int((nf+2)/2) * (W/nf + 0.18u)' nrd='0.18u / W' nrs='0.18u / W'
+ sa=0 sb=0 sd=0 m=1
XM118 net95 VG net103 VB nfet_03v3 L=2u W=2u nf=1 ad='int((nf+1)/2) * W/nf * 0.18u' as='int((nf+2)/2) * W/nf * 0.18u'
+ pd='2*int((nf+1)/2) * (W/nf + 0.18u)' ps='2*int((nf+2)/2) * (W/nf + 0.18u)' nrd='0.18u / W' nrs='0.18u / W'
+ sa=0 sb=0 sd=0 m=1
XM119 net88 VG net96 VB nfet_03v3 L=2u W=2u nf=1 ad='int((nf+1)/2) * W/nf * 0.18u' as='int((nf+2)/2) * W/nf * 0.18u'
+ pd='2*int((nf+1)/2) * (W/nf + 0.18u)' ps='2*int((nf+2)/2) * (W/nf + 0.18u)' nrd='0.18u / W' nrs='0.18u / W'
+ sa=0 sb=0 sd=0 m=1
XM120 net96 VG net104 VB nfet_03v3 L=2u W=2u nf=1 ad='int((nf+1)/2) * W/nf * 0.18u' as='int((nf+2)/2) * W/nf * 0.18u'
+ pd='2*int((nf+1)/2) * (W/nf + 0.18u)' ps='2*int((nf+2)/2) * (W/nf + 0.18u)' nrd='0.18u / W' nrs='0.18u / W'
+ sa=0 sb=0 sd=0 m=1
XM121 net82 VG net97 VB nfet_03v3 L=2u W=2u nf=1 ad='int((nf+1)/2) * W/nf * 0.18u' as='int((nf+2)/2) * W/nf * 0.18u'
+ pd='2*int((nf+1)/2) * (W/nf + 0.18u)' ps='2*int((nf+2)/2) * (W/nf + 0.18u)' nrd='0.18u / W' nrs='0.18u / W'
+ sa=0 sb=0 sd=0 m=1
XM122 net97 VG net98 VB nfet_03v3 L=2u W=2u nf=1 ad='int((nf+1)/2) * W/nf * 0.18u' as='int((nf+2)/2) * W/nf * 0.18u'
+ pd='2*int((nf+1)/2) * (W/nf + 0.18u)' ps='2*int((nf+2)/2) * (W/nf + 0.18u)' nrd='0.18u / W' nrs='0.18u / W'
+ sa=0 sb=0 sd=0 m=1
XM123 net90 VG net123 VB nfet_03v3 L=2u W=2u nf=1 ad='int((nf+1)/2) * W/nf * 0.18u' as='int((nf+2)/2) * W/nf * 0.18u'
+ pd='2*int((nf+1)/2) * (W/nf + 0.18u)' ps='2*int((nf+2)/2) * (W/nf + 0.18u)' nrd='0.18u / W' nrs='0.18u / W'
+ sa=0 sb=0 sd=0 m=1
XM124 net99 VG net125 VB nfet_03v3 L=2u W=2u nf=1 ad='int((nf+1)/2) * W/nf * 0.18u' as='int((nf+2)/2) * W/nf * 0.18u'
+ pd='2*int((nf+1)/2) * (W/nf + 0.18u)' ps='2*int((nf+2)/2) * (W/nf + 0.18u)' nrd='0.18u / W' nrs='0.18u / W'
+ sa=0 sb=0 sd=0 m=1
XM125 net100 VG net126 VB nfet_03v3 L=2u W=2u nf=1 ad='int((nf+1)/2) * W/nf * 0.18u' as='int((nf+2)/2) * W/nf * 0.18u'
+ pd='2*int((nf+1)/2) * (W/nf + 0.18u)' ps='2*int((nf+2)/2) * (W/nf + 0.18u)' nrd='0.18u / W' nrs='0.18u / W'
+ sa=0 sb=0 sd=0 m=1
XM126 net101 VG net127 VB nfet_03v3 L=2u W=2u nf=1 ad='int((nf+1)/2) * W/nf * 0.18u' as='int((nf+2)/2) * W/nf * 0.18u'
+ pd='2*int((nf+1)/2) * (W/nf + 0.18u)' ps='2*int((nf+2)/2) * (W/nf + 0.18u)' nrd='0.18u / W' nrs='0.18u / W'
+ sa=0 sb=0 sd=0 m=1
XM127 net102 VG net128 VB nfet_03v3 L=2u W=2u nf=1 ad='int((nf+1)/2) * W/nf * 0.18u' as='int((nf+2)/2) * W/nf * 0.18u'
+ pd='2*int((nf+1)/2) * (W/nf + 0.18u)' ps='2*int((nf+2)/2) * (W/nf + 0.18u)' nrd='0.18u / W' nrs='0.18u / W'
+ sa=0 sb=0 sd=0 m=1
XM128 net103 VG net129 VB nfet_03v3 L=2u W=2u nf=1 ad='int((nf+1)/2) * W/nf * 0.18u' as='int((nf+2)/2) * W/nf * 0.18u'
+ pd='2*int((nf+1)/2) * (W/nf + 0.18u)' ps='2*int((nf+2)/2) * (W/nf + 0.18u)' nrd='0.18u / W' nrs='0.18u / W'
+ sa=0 sb=0 sd=0 m=1
XM129 net104 VG net130 VB nfet_03v3 L=2u W=2u nf=1 ad='int((nf+1)/2) * W/nf * 0.18u' as='int((nf+2)/2) * W/nf * 0.18u'
+ pd='2*int((nf+1)/2) * (W/nf + 0.18u)' ps='2*int((nf+2)/2) * (W/nf + 0.18u)' nrd='0.18u / W' nrs='0.18u / W'
+ sa=0 sb=0 sd=0 m=1
XM130 net98 VG net124 VB nfet_03v3 L=2u W=2u nf=1 ad='int((nf+1)/2) * W/nf * 0.18u' as='int((nf+2)/2) * W/nf * 0.18u'
+ pd='2*int((nf+1)/2) * (W/nf + 0.18u)' ps='2*int((nf+2)/2) * (W/nf + 0.18u)' nrd='0.18u / W' nrs='0.18u / W'
+ sa=0 sb=0 sd=0 m=1
XM131 net122 VG VS VB nfet_03v3 L=2u W=2u nf=1 ad='int((nf+1)/2) * W/nf * 0.18u' as='int((nf+2)/2) * W/nf * 0.18u'
+ pd='2*int((nf+1)/2) * (W/nf + 0.18u)' ps='2*int((nf+2)/2) * (W/nf + 0.18u)' nrd='0.18u / W' nrs='0.18u / W'
+ sa=0 sb=0 sd=0 m=1
XM132 net106 VG VS VB nfet_03v3 L=2u W=2u nf=1 ad='int((nf+1)/2) * W/nf * 0.18u' as='int((nf+2)/2) * W/nf * 0.18u'
+ pd='2*int((nf+1)/2) * (W/nf + 0.18u)' ps='2*int((nf+2)/2) * (W/nf + 0.18u)' nrd='0.18u / W' nrs='0.18u / W'
+ sa=0 sb=0 sd=0 m=1
XM133 net107 VG VS VB nfet_03v3 L=2u W=2u nf=1 ad='int((nf+1)/2) * W/nf * 0.18u' as='int((nf+2)/2) * W/nf * 0.18u'
+ pd='2*int((nf+1)/2) * (W/nf + 0.18u)' ps='2*int((nf+2)/2) * (W/nf + 0.18u)' nrd='0.18u / W' nrs='0.18u / W'
+ sa=0 sb=0 sd=0 m=1
XM134 net108 VG VS VB nfet_03v3 L=2u W=2u nf=1 ad='int((nf+1)/2) * W/nf * 0.18u' as='int((nf+2)/2) * W/nf * 0.18u'
+ pd='2*int((nf+1)/2) * (W/nf + 0.18u)' ps='2*int((nf+2)/2) * (W/nf + 0.18u)' nrd='0.18u / W' nrs='0.18u / W'
+ sa=0 sb=0 sd=0 m=1
XM135 net109 VG VS VB nfet_03v3 L=2u W=2u nf=1 ad='int((nf+1)/2) * W/nf * 0.18u' as='int((nf+2)/2) * W/nf * 0.18u'
+ pd='2*int((nf+1)/2) * (W/nf + 0.18u)' ps='2*int((nf+2)/2) * (W/nf + 0.18u)' nrd='0.18u / W' nrs='0.18u / W'
+ sa=0 sb=0 sd=0 m=1
XM136 net110 VG VS VB nfet_03v3 L=2u W=2u nf=1 ad='int((nf+1)/2) * W/nf * 0.18u' as='int((nf+2)/2) * W/nf * 0.18u'
+ pd='2*int((nf+1)/2) * (W/nf + 0.18u)' ps='2*int((nf+2)/2) * (W/nf + 0.18u)' nrd='0.18u / W' nrs='0.18u / W'
+ sa=0 sb=0 sd=0 m=1
XM137 net111 VG VS VB nfet_03v3 L=2u W=2u nf=1 ad='int((nf+1)/2) * W/nf * 0.18u' as='int((nf+2)/2) * W/nf * 0.18u'
+ pd='2*int((nf+1)/2) * (W/nf + 0.18u)' ps='2*int((nf+2)/2) * (W/nf + 0.18u)' nrd='0.18u / W' nrs='0.18u / W'
+ sa=0 sb=0 sd=0 m=1
XM138 net112 VG VS VB nfet_03v3 L=2u W=2u nf=1 ad='int((nf+1)/2) * W/nf * 0.18u' as='int((nf+2)/2) * W/nf * 0.18u'
+ pd='2*int((nf+1)/2) * (W/nf + 0.18u)' ps='2*int((nf+2)/2) * (W/nf + 0.18u)' nrd='0.18u / W' nrs='0.18u / W'
+ sa=0 sb=0 sd=0 m=1
XM139 net113 VG VS VB nfet_03v3 L=2u W=2u nf=1 ad='int((nf+1)/2) * W/nf * 0.18u' as='int((nf+2)/2) * W/nf * 0.18u'
+ pd='2*int((nf+1)/2) * (W/nf + 0.18u)' ps='2*int((nf+2)/2) * (W/nf + 0.18u)' nrd='0.18u / W' nrs='0.18u / W'
+ sa=0 sb=0 sd=0 m=1
XM140 net114 VG VS VB nfet_03v3 L=2u W=2u nf=1 ad='int((nf+1)/2) * W/nf * 0.18u' as='int((nf+2)/2) * W/nf * 0.18u'
+ pd='2*int((nf+1)/2) * (W/nf + 0.18u)' ps='2*int((nf+2)/2) * (W/nf + 0.18u)' nrd='0.18u / W' nrs='0.18u / W'
+ sa=0 sb=0 sd=0 m=1
XM141 net105 VG VS VB nfet_03v3 L=2u W=2u nf=1 ad='int((nf+1)/2) * W/nf * 0.18u' as='int((nf+2)/2) * W/nf * 0.18u'
+ pd='2*int((nf+1)/2) * (W/nf + 0.18u)' ps='2*int((nf+2)/2) * (W/nf + 0.18u)' nrd='0.18u / W' nrs='0.18u / W'
+ sa=0 sb=0 sd=0 m=1
XM142 net116 VG VS VB nfet_03v3 L=2u W=2u nf=1 ad='int((nf+1)/2) * W/nf * 0.18u' as='int((nf+2)/2) * W/nf * 0.18u'
+ pd='2*int((nf+1)/2) * (W/nf + 0.18u)' ps='2*int((nf+2)/2) * (W/nf + 0.18u)' nrd='0.18u / W' nrs='0.18u / W'
+ sa=0 sb=0 sd=0 m=1
XM143 net117 VG VS VB nfet_03v3 L=2u W=2u nf=1 ad='int((nf+1)/2) * W/nf * 0.18u' as='int((nf+2)/2) * W/nf * 0.18u'
+ pd='2*int((nf+1)/2) * (W/nf + 0.18u)' ps='2*int((nf+2)/2) * (W/nf + 0.18u)' nrd='0.18u / W' nrs='0.18u / W'
+ sa=0 sb=0 sd=0 m=1
XM144 net118 VG VS VB nfet_03v3 L=2u W=2u nf=1 ad='int((nf+1)/2) * W/nf * 0.18u' as='int((nf+2)/2) * W/nf * 0.18u'
+ pd='2*int((nf+1)/2) * (W/nf + 0.18u)' ps='2*int((nf+2)/2) * (W/nf + 0.18u)' nrd='0.18u / W' nrs='0.18u / W'
+ sa=0 sb=0 sd=0 m=1
XM145 net119 VG VS VB nfet_03v3 L=2u W=2u nf=1 ad='int((nf+1)/2) * W/nf * 0.18u' as='int((nf+2)/2) * W/nf * 0.18u'
+ pd='2*int((nf+1)/2) * (W/nf + 0.18u)' ps='2*int((nf+2)/2) * (W/nf + 0.18u)' nrd='0.18u / W' nrs='0.18u / W'
+ sa=0 sb=0 sd=0 m=1
XM146 net120 VG VS VB nfet_03v3 L=2u W=2u nf=1 ad='int((nf+1)/2) * W/nf * 0.18u' as='int((nf+2)/2) * W/nf * 0.18u'
+ pd='2*int((nf+1)/2) * (W/nf + 0.18u)' ps='2*int((nf+2)/2) * (W/nf + 0.18u)' nrd='0.18u / W' nrs='0.18u / W'
+ sa=0 sb=0 sd=0 m=1
XM147 net121 VG VS VB nfet_03v3 L=2u W=2u nf=1 ad='int((nf+1)/2) * W/nf * 0.18u' as='int((nf+2)/2) * W/nf * 0.18u'
+ pd='2*int((nf+1)/2) * (W/nf + 0.18u)' ps='2*int((nf+2)/2) * (W/nf + 0.18u)' nrd='0.18u / W' nrs='0.18u / W'
+ sa=0 sb=0 sd=0 m=1
XM148 net115 VG VS VB nfet_03v3 L=2u W=2u nf=1 ad='int((nf+1)/2) * W/nf * 0.18u' as='int((nf+2)/2) * W/nf * 0.18u'
+ pd='2*int((nf+1)/2) * (W/nf + 0.18u)' ps='2*int((nf+2)/2) * (W/nf + 0.18u)' nrd='0.18u / W' nrs='0.18u / W'
+ sa=0 sb=0 sd=0 m=1
XM149 net123 VG VS VB nfet_03v3 L=2u W=2u nf=1 ad='int((nf+1)/2) * W/nf * 0.18u' as='int((nf+2)/2) * W/nf * 0.18u'
+ pd='2*int((nf+1)/2) * (W/nf + 0.18u)' ps='2*int((nf+2)/2) * (W/nf + 0.18u)' nrd='0.18u / W' nrs='0.18u / W'
+ sa=0 sb=0 sd=0 m=1
XM150 net125 VG VS VB nfet_03v3 L=2u W=2u nf=1 ad='int((nf+1)/2) * W/nf * 0.18u' as='int((nf+2)/2) * W/nf * 0.18u'
+ pd='2*int((nf+1)/2) * (W/nf + 0.18u)' ps='2*int((nf+2)/2) * (W/nf + 0.18u)' nrd='0.18u / W' nrs='0.18u / W'
+ sa=0 sb=0 sd=0 m=1
XM151 net126 VG VS VB nfet_03v3 L=2u W=2u nf=1 ad='int((nf+1)/2) * W/nf * 0.18u' as='int((nf+2)/2) * W/nf * 0.18u'
+ pd='2*int((nf+1)/2) * (W/nf + 0.18u)' ps='2*int((nf+2)/2) * (W/nf + 0.18u)' nrd='0.18u / W' nrs='0.18u / W'
+ sa=0 sb=0 sd=0 m=1
XM152 net127 VG VS VB nfet_03v3 L=2u W=2u nf=1 ad='int((nf+1)/2) * W/nf * 0.18u' as='int((nf+2)/2) * W/nf * 0.18u'
+ pd='2*int((nf+1)/2) * (W/nf + 0.18u)' ps='2*int((nf+2)/2) * (W/nf + 0.18u)' nrd='0.18u / W' nrs='0.18u / W'
+ sa=0 sb=0 sd=0 m=1
XM153 net128 VG VS VB nfet_03v3 L=2u W=2u nf=1 ad='int((nf+1)/2) * W/nf * 0.18u' as='int((nf+2)/2) * W/nf * 0.18u'
+ pd='2*int((nf+1)/2) * (W/nf + 0.18u)' ps='2*int((nf+2)/2) * (W/nf + 0.18u)' nrd='0.18u / W' nrs='0.18u / W'
+ sa=0 sb=0 sd=0 m=1
XM154 net129 VG VS VB nfet_03v3 L=2u W=2u nf=1 ad='int((nf+1)/2) * W/nf * 0.18u' as='int((nf+2)/2) * W/nf * 0.18u'
+ pd='2*int((nf+1)/2) * (W/nf + 0.18u)' ps='2*int((nf+2)/2) * (W/nf + 0.18u)' nrd='0.18u / W' nrs='0.18u / W'
+ sa=0 sb=0 sd=0 m=1
XM155 net130 VG VS VB nfet_03v3 L=2u W=2u nf=1 ad='int((nf+1)/2) * W/nf * 0.18u' as='int((nf+2)/2) * W/nf * 0.18u'
+ pd='2*int((nf+1)/2) * (W/nf + 0.18u)' ps='2*int((nf+2)/2) * (W/nf + 0.18u)' nrd='0.18u / W' nrs='0.18u / W'
+ sa=0 sb=0 sd=0 m=1
XM156 net124 VG VS VB nfet_03v3 L=2u W=2u nf=1 ad='int((nf+1)/2) * W/nf * 0.18u' as='int((nf+2)/2) * W/nf * 0.18u'
+ pd='2*int((nf+1)/2) * (W/nf + 0.18u)' ps='2*int((nf+2)/2) * (W/nf + 0.18u)' nrd='0.18u / W' nrs='0.18u / W'
+ sa=0 sb=0 sd=0 m=1
XM157 VD VG net131 VB nfet_03v3 L=2u W=2u nf=1 ad='int((nf+1)/2) * W/nf * 0.18u' as='int((nf+2)/2) * W/nf * 0.18u'
+ pd='2*int((nf+1)/2) * (W/nf + 0.18u)' ps='2*int((nf+2)/2) * (W/nf + 0.18u)' nrd='0.18u / W' nrs='0.18u / W'
+ sa=0 sb=0 sd=0 m=1
XM158 net131 VG net134 VB nfet_03v3 L=2u W=2u nf=1 ad='int((nf+1)/2) * W/nf * 0.18u' as='int((nf+2)/2) * W/nf * 0.18u'
+ pd='2*int((nf+1)/2) * (W/nf + 0.18u)' ps='2*int((nf+2)/2) * (W/nf + 0.18u)' nrd='0.18u / W' nrs='0.18u / W'
+ sa=0 sb=0 sd=0 m=1
XM159 VD VG net132 VB nfet_03v3 L=2u W=2u nf=1 ad='int((nf+1)/2) * W/nf * 0.18u' as='int((nf+2)/2) * W/nf * 0.18u'
+ pd='2*int((nf+1)/2) * (W/nf + 0.18u)' ps='2*int((nf+2)/2) * (W/nf + 0.18u)' nrd='0.18u / W' nrs='0.18u / W'
+ sa=0 sb=0 sd=0 m=1
XM160 net132 VG net133 VB nfet_03v3 L=2u W=2u nf=1 ad='int((nf+1)/2) * W/nf * 0.18u' as='int((nf+2)/2) * W/nf * 0.18u'
+ pd='2*int((nf+1)/2) * (W/nf + 0.18u)' ps='2*int((nf+2)/2) * (W/nf + 0.18u)' nrd='0.18u / W' nrs='0.18u / W'
+ sa=0 sb=0 sd=0 m=1
XM161 net134 VG net135 VB nfet_03v3 L=2u W=2u nf=1 ad='int((nf+1)/2) * W/nf * 0.18u' as='int((nf+2)/2) * W/nf * 0.18u'
+ pd='2*int((nf+1)/2) * (W/nf + 0.18u)' ps='2*int((nf+2)/2) * (W/nf + 0.18u)' nrd='0.18u / W' nrs='0.18u / W'
+ sa=0 sb=0 sd=0 m=1
XM162 net135 VG net138 VB nfet_03v3 L=2u W=2u nf=1 ad='int((nf+1)/2) * W/nf * 0.18u' as='int((nf+2)/2) * W/nf * 0.18u'
+ pd='2*int((nf+1)/2) * (W/nf + 0.18u)' ps='2*int((nf+2)/2) * (W/nf + 0.18u)' nrd='0.18u / W' nrs='0.18u / W'
+ sa=0 sb=0 sd=0 m=1
XM163 net133 VG net136 VB nfet_03v3 L=2u W=2u nf=1 ad='int((nf+1)/2) * W/nf * 0.18u' as='int((nf+2)/2) * W/nf * 0.18u'
+ pd='2*int((nf+1)/2) * (W/nf + 0.18u)' ps='2*int((nf+2)/2) * (W/nf + 0.18u)' nrd='0.18u / W' nrs='0.18u / W'
+ sa=0 sb=0 sd=0 m=1
XM164 net136 VG net137 VB nfet_03v3 L=2u W=2u nf=1 ad='int((nf+1)/2) * W/nf * 0.18u' as='int((nf+2)/2) * W/nf * 0.18u'
+ pd='2*int((nf+1)/2) * (W/nf + 0.18u)' ps='2*int((nf+2)/2) * (W/nf + 0.18u)' nrd='0.18u / W' nrs='0.18u / W'
+ sa=0 sb=0 sd=0 m=1
XM165 net138 VG net140 VB nfet_03v3 L=2u W=2u nf=1 ad='int((nf+1)/2) * W/nf * 0.18u' as='int((nf+2)/2) * W/nf * 0.18u'
+ pd='2*int((nf+1)/2) * (W/nf + 0.18u)' ps='2*int((nf+2)/2) * (W/nf + 0.18u)' nrd='0.18u / W' nrs='0.18u / W'
+ sa=0 sb=0 sd=0 m=1
XM166 net137 VG net139 VB nfet_03v3 L=2u W=2u nf=1 ad='int((nf+1)/2) * W/nf * 0.18u' as='int((nf+2)/2) * W/nf * 0.18u'
+ pd='2*int((nf+1)/2) * (W/nf + 0.18u)' ps='2*int((nf+2)/2) * (W/nf + 0.18u)' nrd='0.18u / W' nrs='0.18u / W'
+ sa=0 sb=0 sd=0 m=1
XM167 net140 VG VS VB nfet_03v3 L=2u W=2u nf=1 ad='int((nf+1)/2) * W/nf * 0.18u' as='int((nf+2)/2) * W/nf * 0.18u'
+ pd='2*int((nf+1)/2) * (W/nf + 0.18u)' ps='2*int((nf+2)/2) * (W/nf + 0.18u)' nrd='0.18u / W' nrs='0.18u / W'
+ sa=0 sb=0 sd=0 m=1
XM168 net139 VG VS VB nfet_03v3 L=2u W=2u nf=1 ad='int((nf+1)/2) * W/nf * 0.18u' as='int((nf+2)/2) * W/nf * 0.18u'
+ pd='2*int((nf+1)/2) * (W/nf + 0.18u)' ps='2*int((nf+2)/2) * (W/nf + 0.18u)' nrd='0.18u / W' nrs='0.18u / W'
+ sa=0 sb=0 sd=0 m=1
**.ends
.end
